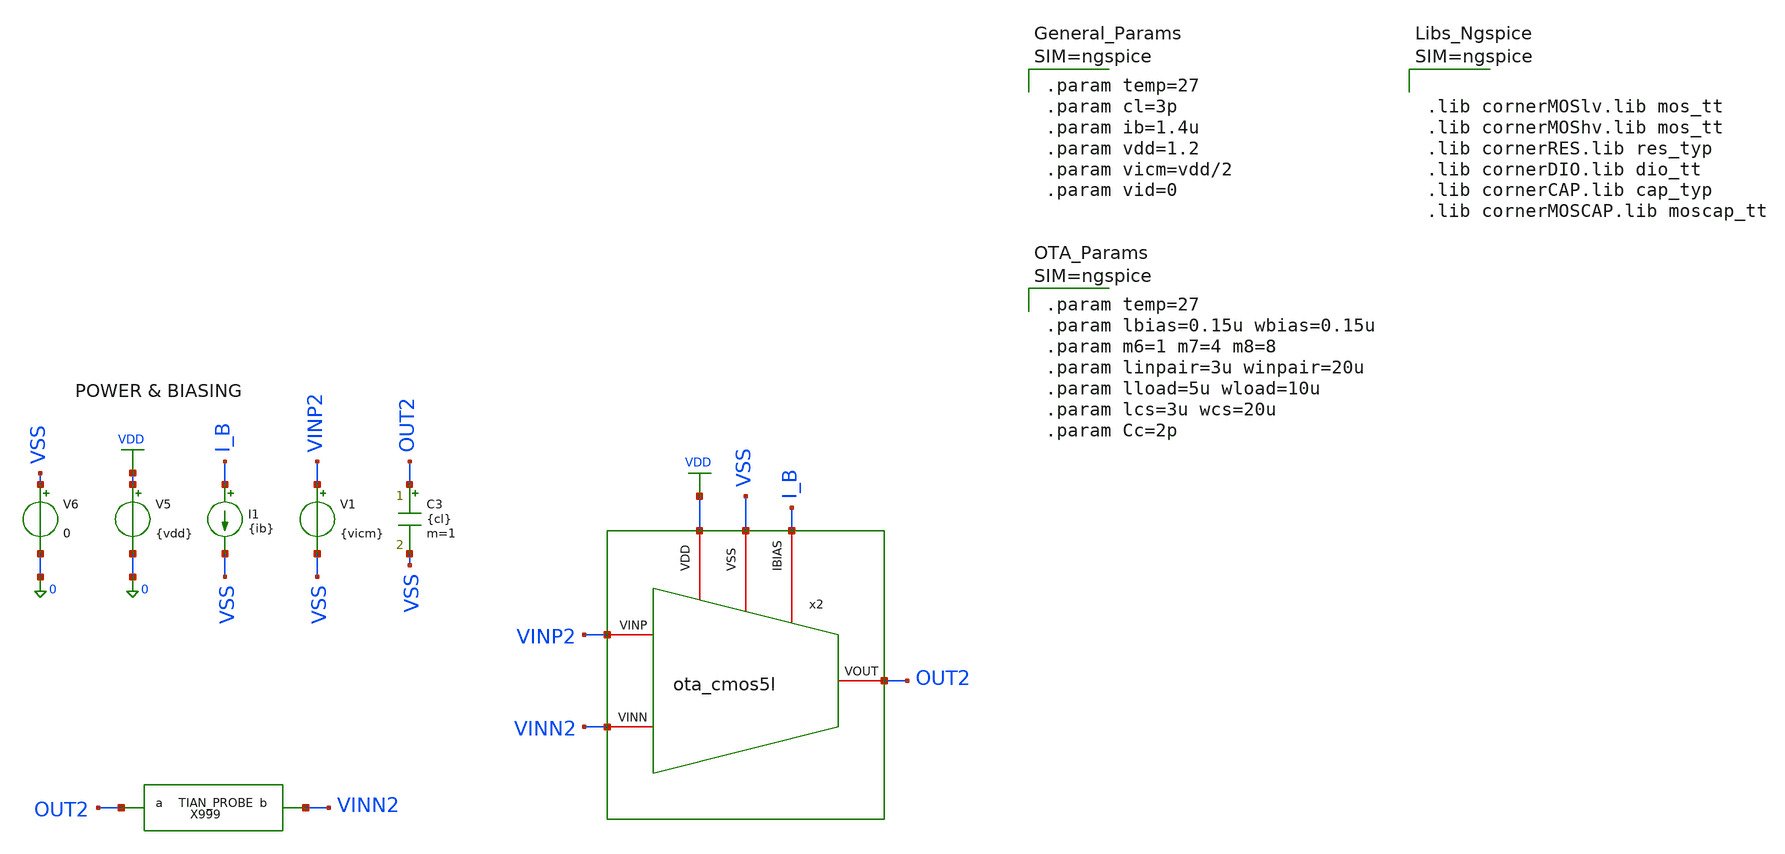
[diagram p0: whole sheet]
** sch_path: xschem/ota_cmos5l/tb/tb_ota_cmos5l_ac/tb_ota_cmos5l_ac.sch
**.subckt tb_ota_cmos5l_ac
I1 I_B VSS {ib}
V5 VDD 0 {vdd}
V6 VSS 0 0
V1 VINP2 VSS {vicm}
C3 OUT2 VSS {cl} m=1
x2 VSS I_B VDD VINN2 VINP2 OUT2 ota_cmos5l
X999 OUT2 VINN2 loopgainprobe
**** begin user architecture code



.lib cornerMOSlv.lib mos_tt
.lib cornerMOShv.lib mos_tt
.lib cornerRES.lib res_typ
.lib cornerDIO.lib dio_tt
.lib cornerCAP.lib cap_typ
.lib cornerMOSCAP.lib moscap_tt





.subckt loopgainprobe a b
Ii 0 x DC 0 AC 0
Vi x a DC 0 AC 1
Vnodebuffer b x 0
.ends loopgainprobe

.func tian_loop() {1/(1/(2*(ac1.i(v.x999.Vi)*ac2.v(x999.x)-ac1.v(x999.x)*ac2.i(v.x999.Vi))+ac1.v(x999.x)+ac2.i(v.x999.Vi))-1)}





.param temp=27
.param cl=3p
.param ib=1.4u
.param vdd=1.2
.param vicm=vdd/2
.param vid=0





.param temp=27
.param lbias=0.15u wbias=0.15u
.param m6=1 m7=4 m8=8
.param linpair=3u winpair=20u
.param lload=5u wload=10u
.param lcs=3u wcs=20u
.param Cc=2p





.control
save all
shell mkdir -p result

* 1st Injection: AC Voltage + 1st AC sim
alter i.x999.ii acmag=0
alter v.x999.vi acmag=1
ac dec 50 1 10G

* 2nd Injection: AC Current + 2nd AC sim
alter i.x999.ii acmag=1
alter v.x999.vi acmag=0
ac dec 50 1 10G

* Set default plot to 1st AC sim
setplot ac1

let t_gain = tian_loop()
let loop_mag = db(t_gain)
let loop_ph = 180 + (180 * cph(t_gain) / pi)

meas ac dc_gain find loop_mag at=10
let dc_gain_lin = 10^(dc_gain / 20)
let target_3db = dc_gain - 3
meas ac f_3db when loop_mag=target_3db
meas ac ph_3db find loop_ph when loop_mag=target_3db

meas ac ugbw when loop_mag=0
meas ac pm find loop_ph when loop_mag=0

meas ac f_180 when loop_ph=0
meas ac gain_margin find loop_mag when loop_ph=0
let gm_db=-gain_margin

let gbw_calc=dc_gain_lin * f_3db

write ./result/tb_cg_ota_ac.raw loop_mag loop_ph

echo "======================================================="
echo " DC Gain (dB): " $&dc_gain " dB"
echo " DC Gain (Lin): " $&dc_gain_lin " V/V"
echo " Bandwidth 3dB (f_3dB): " $&f_3db " Hz"
echo " Phase 3dB (f_3dB): " $&ph_3db " deg (Ideally, ~135 deg)"
echo " Unity-Gain BW (UGBW): " $&ugbw " Hz"
echo " Phase Margin (PM): " $&pm " deg (Ideally, > 60 deg)"
echo " Gain Margin (GM): " $&gm_db " dB"
echo " Phase Crossover (f_180): " $&f_180 " Hz"
echo " GBW Product (PM): " $&gbw_calc " Hz"


plot re(loop_mag) re(loop_ph) xlog

.endc


**** end user architecture code
**.ends

* expanding   symbol:  /foss/designs/sg13cmos5l_spma_ip__instramp/xschem/ota_cmos5l/ota_cmos5l.sym #
*+ of pins=6
** sym_path: xschem/output_buffer/ota_cmos5l.sym
** sch_path: xschem/output_buffer/ota_cmos5l.sch
.subckt ota_cmos5l VSS IBIAS VDD VINN VINP VOUT
*.iopin IBIAS
*.iopin VDD
*.iopin VSS
*.iopin VOUT
*.iopin VINP
*.iopin VINN
XM6 IBIAS IBIAS VDD VDD sg13_lv_pmos w={wbias} l={lbias} ng=1 m={m6} mm_ok=1
XM7 net1 IBIAS VDD VDD sg13_lv_pmos w={wbias} l={lbias} ng=1 m={m7} mm_ok=1
XM8 VOUT IBIAS VDD VDD sg13_lv_pmos w={wbias} l={lbias} ng=1 m={m8} mm_ok=1
XM1 net2 VINN net1 VDD sg13_lv_pmos w={winpair} l={linpair} ng=1 m=1 mm_ok=1
XM2 net3 VINP net1 VDD sg13_lv_pmos w={winpair} l={linpair} ng=1 m=1 mm_ok=1
XM3 net2 net2 VSS VSS sg13_lv_nmos w={wload} l={lload} ng=1 m=1 mm_ok=1
XM4 net3 net2 VSS VSS sg13_lv_nmos w={wload} l={lload} ng=1 m=1 mm_ok=1
XM5 VOUT net3 VSS VSS sg13_lv_nmos w={wcs} l={lcs} ng=1 m=1 mm_ok=1
XR1 net3 net4 VSS rhigh w=0.5e-6 l=1.95e-6 m=1 b=0 mm_ok=1
.save v(vinp)
.save v(vinn)
.save v(vout)
XC2 VOUT net4 cap_cmomi w=15e-6 l=15e-6 mmin=1 mmax=4 feed=double subblock=0 m=5 mm_ok=1
**** begin user architecture code


.param temp=27
.param lbias=0.15u wbias=0.15u
.param m6=1 m7=4 m8=8
.param linpair=3u winpair=20u
.param lload=5u wload=10u
.param lcs=3u wcs=20u
.param Cc=2p



**** end user architecture code
XC1 VOUT net4 cap_cmomi w=15e-6 l=15e-6 mmin=1 mmax=4 feed=double subblock=0 m=4 mm_ok=1
.ends

.GLOBAL VDD
.end
